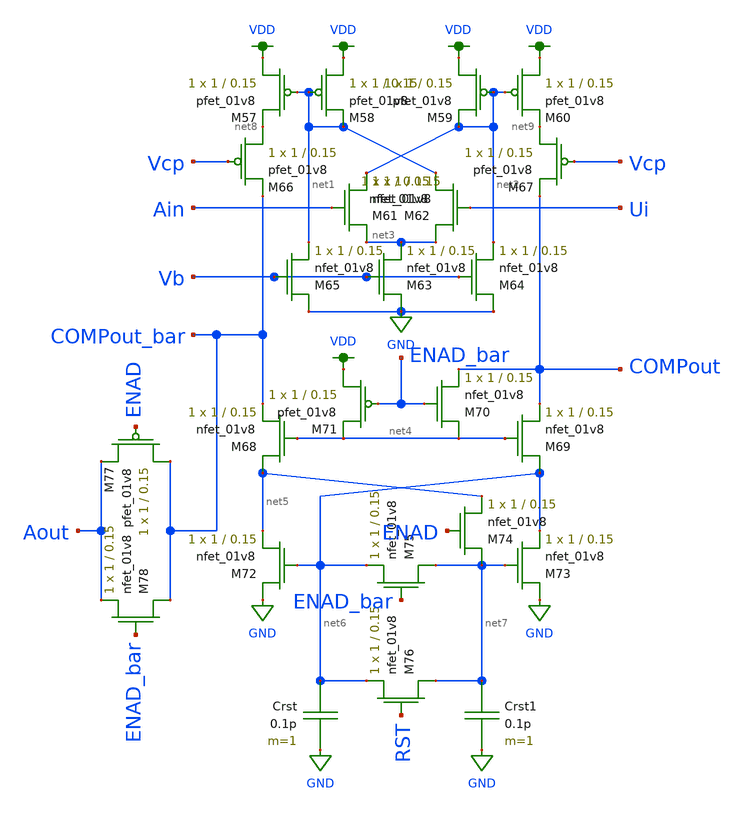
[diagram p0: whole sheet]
** sch_path: schematics/comp_report.sch
**.subckt comp_report
XM57 VDD net1 net8 VDD sky130_fd_pr__pfet_01v8 L=0.15 W=1 nf=1 ad='int((nf+1)/2) * W/nf * 0.29' as='int((nf+2)/2) * W/nf * 0.29'
+ pd='2*int((nf+1)/2) * (W/nf + 0.29)' ps='2*int((nf+2)/2) * (W/nf + 0.29)' nrd='0.29 / W' nrs='0.29 / W'
+ sa=0 sb=0 sd=0 mult=1 m=1
XM58 VDD net1 net1 VDD sky130_fd_pr__pfet_01v8 L=0.15 W=1 nf=1 ad='int((nf+1)/2) * W/nf * 0.29' as='int((nf+2)/2) * W/nf * 0.29'
+ pd='2*int((nf+1)/2) * (W/nf + 0.29)' ps='2*int((nf+2)/2) * (W/nf + 0.29)' nrd='0.29 / W' nrs='0.29 / W'
+ sa=0 sb=0 sd=0 mult=1 m=1
XM59 VDD net2 net2 VDD sky130_fd_pr__pfet_01v8 L=0.15 W=1 nf=1 ad='int((nf+1)/2) * W/nf * 0.29' as='int((nf+2)/2) * W/nf * 0.29'
+ pd='2*int((nf+1)/2) * (W/nf + 0.29)' ps='2*int((nf+2)/2) * (W/nf + 0.29)' nrd='0.29 / W' nrs='0.29 / W'
+ sa=0 sb=0 sd=0 mult=1 m=1
XM60 VDD net2 net9 VDD sky130_fd_pr__pfet_01v8 L=0.15 W=1 nf=1 ad='int((nf+1)/2) * W/nf * 0.29' as='int((nf+2)/2) * W/nf * 0.29'
+ pd='2*int((nf+1)/2) * (W/nf + 0.29)' ps='2*int((nf+2)/2) * (W/nf + 0.29)' nrd='0.29 / W' nrs='0.29 / W'
+ sa=0 sb=0 sd=0 mult=1 m=1
XM61 net3 Ain net2 GND sky130_fd_pr__nfet_01v8 L=0.15 W=1 nf=1 ad='int((nf+1)/2) * W/nf * 0.29' as='int((nf+2)/2) * W/nf * 0.29'
+ pd='2*int((nf+1)/2) * (W/nf + 0.29)' ps='2*int((nf+2)/2) * (W/nf + 0.29)' nrd='0.29 / W' nrs='0.29 / W'
+ sa=0 sb=0 sd=0 mult=1 m=1
XM62 net3 Ui net1 GND sky130_fd_pr__nfet_01v8 L=0.15 W=1 nf=1 ad='int((nf+1)/2) * W/nf * 0.29' as='int((nf+2)/2) * W/nf * 0.29'
+ pd='2*int((nf+1)/2) * (W/nf + 0.29)' ps='2*int((nf+2)/2) * (W/nf + 0.29)' nrd='0.29 / W' nrs='0.29 / W'
+ sa=0 sb=0 sd=0 mult=1 m=1
XM63 GND Vb net3 GND sky130_fd_pr__nfet_01v8 L=0.15 W=1 nf=1 ad='int((nf+1)/2) * W/nf * 0.29' as='int((nf+2)/2) * W/nf * 0.29'
+ pd='2*int((nf+1)/2) * (W/nf + 0.29)' ps='2*int((nf+2)/2) * (W/nf + 0.29)' nrd='0.29 / W' nrs='0.29 / W'
+ sa=0 sb=0 sd=0 mult=1 m=1
XM64 GND Vb net2 GND sky130_fd_pr__nfet_01v8 L=0.15 W=1 nf=1 ad='int((nf+1)/2) * W/nf * 0.29' as='int((nf+2)/2) * W/nf * 0.29'
+ pd='2*int((nf+1)/2) * (W/nf + 0.29)' ps='2*int((nf+2)/2) * (W/nf + 0.29)' nrd='0.29 / W' nrs='0.29 / W'
+ sa=0 sb=0 sd=0 mult=1 m=1
XM65 GND Vb net1 GND sky130_fd_pr__nfet_01v8 L=0.15 W=1 nf=1 ad='int((nf+1)/2) * W/nf * 0.29' as='int((nf+2)/2) * W/nf * 0.29'
+ pd='2*int((nf+1)/2) * (W/nf + 0.29)' ps='2*int((nf+2)/2) * (W/nf + 0.29)' nrd='0.29 / W' nrs='0.29 / W'
+ sa=0 sb=0 sd=0 mult=1 m=1
XM66 net8 Vcp COMPout_bar VDD sky130_fd_pr__pfet_01v8 L=0.15 W=1 nf=1 ad='int((nf+1)/2) * W/nf * 0.29'
+ as='int((nf+2)/2) * W/nf * 0.29' pd='2*int((nf+1)/2) * (W/nf + 0.29)' ps='2*int((nf+2)/2) * (W/nf + 0.29)'
+ nrd='0.29 / W' nrs='0.29 / W' sa=0 sb=0 sd=0 mult=1 m=1
XM67 net9 Vcp COMPout VDD sky130_fd_pr__pfet_01v8 L=0.15 W=1 nf=1 ad='int((nf+1)/2) * W/nf * 0.29' as='int((nf+2)/2) * W/nf * 0.29'
+ pd='2*int((nf+1)/2) * (W/nf + 0.29)' ps='2*int((nf+2)/2) * (W/nf + 0.29)' nrd='0.29 / W' nrs='0.29 / W'
+ sa=0 sb=0 sd=0 mult=1 m=1
XM68 net5 net4 COMPout_bar GND sky130_fd_pr__nfet_01v8 L=0.15 W=1 nf=1 ad='int((nf+1)/2) * W/nf * 0.29'
+ as='int((nf+2)/2) * W/nf * 0.29' pd='2*int((nf+1)/2) * (W/nf + 0.29)' ps='2*int((nf+2)/2) * (W/nf + 0.29)'
+ nrd='0.29 / W' nrs='0.29 / W' sa=0 sb=0 sd=0 mult=1 m=1
XM69 net6 net4 COMPout GND sky130_fd_pr__nfet_01v8 L=0.15 W=1 nf=1 ad='int((nf+1)/2) * W/nf * 0.29' as='int((nf+2)/2) * W/nf * 0.29'
+ pd='2*int((nf+1)/2) * (W/nf + 0.29)' ps='2*int((nf+2)/2) * (W/nf + 0.29)' nrd='0.29 / W' nrs='0.29 / W'
+ sa=0 sb=0 sd=0 mult=1 m=1
XM70 net4 ENAD_bar COMPout GND sky130_fd_pr__nfet_01v8 L=0.15 W=1 nf=1 ad='int((nf+1)/2) * W/nf * 0.29'
+ as='int((nf+2)/2) * W/nf * 0.29' pd='2*int((nf+1)/2) * (W/nf + 0.29)' ps='2*int((nf+2)/2) * (W/nf + 0.29)'
+ nrd='0.29 / W' nrs='0.29 / W' sa=0 sb=0 sd=0 mult=1 m=1
XM71 VDD ENAD_bar net4 VDD sky130_fd_pr__pfet_01v8 L=0.15 W=1 nf=1 ad='int((nf+1)/2) * W/nf * 0.29' as='int((nf+2)/2) * W/nf * 0.29'
+ pd='2*int((nf+1)/2) * (W/nf + 0.29)' ps='2*int((nf+2)/2) * (W/nf + 0.29)' nrd='0.29 / W' nrs='0.29 / W'
+ sa=0 sb=0 sd=0 mult=1 m=1
XM72 GND net6 net5 GND sky130_fd_pr__nfet_01v8 L=0.15 W=1 nf=1 ad='int((nf+1)/2) * W/nf * 0.29' as='int((nf+2)/2) * W/nf * 0.29'
+ pd='2*int((nf+1)/2) * (W/nf + 0.29)' ps='2*int((nf+2)/2) * (W/nf + 0.29)' nrd='0.29 / W' nrs='0.29 / W'
+ sa=0 sb=0 sd=0 mult=1 m=1
XM73 GND net7 net6 GND sky130_fd_pr__nfet_01v8 L=0.15 W=1 nf=1 ad='int((nf+1)/2) * W/nf * 0.29' as='int((nf+2)/2) * W/nf * 0.29'
+ pd='2*int((nf+1)/2) * (W/nf + 0.29)' ps='2*int((nf+2)/2) * (W/nf + 0.29)' nrd='0.29 / W' nrs='0.29 / W'
+ sa=0 sb=0 sd=0 mult=1 m=1
XM74 net7 ENAD net5 GND sky130_fd_pr__nfet_01v8 L=0.15 W=1 nf=1 ad='int((nf+1)/2) * W/nf * 0.29' as='int((nf+2)/2) * W/nf * 0.29'
+ pd='2*int((nf+1)/2) * (W/nf + 0.29)' ps='2*int((nf+2)/2) * (W/nf + 0.29)' nrd='0.29 / W' nrs='0.29 / W'
+ sa=0 sb=0 sd=0 mult=1 m=1
XM75 net7 ENAD_bar net6 GND sky130_fd_pr__nfet_01v8 L=0.15 W=1 nf=1 ad='int((nf+1)/2) * W/nf * 0.29'
+ as='int((nf+2)/2) * W/nf * 0.29' pd='2*int((nf+1)/2) * (W/nf + 0.29)' ps='2*int((nf+2)/2) * (W/nf + 0.29)'
+ nrd='0.29 / W' nrs='0.29 / W' sa=0 sb=0 sd=0 mult=1 m=1
Crst net6 GND 0.1p m=1
XM76 net7 RST net6 GND sky130_fd_pr__nfet_01v8 L=0.15 W=1 nf=1 ad='int((nf+1)/2) * W/nf * 0.29' as='int((nf+2)/2) * W/nf * 0.29'
+ pd='2*int((nf+1)/2) * (W/nf + 0.29)' ps='2*int((nf+2)/2) * (W/nf + 0.29)' nrd='0.29 / W' nrs='0.29 / W'
+ sa=0 sb=0 sd=0 mult=1 m=1
Crst1 net7 GND 0.1p m=1
XM77 COMPout_bar ENAD Aout VDD sky130_fd_pr__pfet_01v8 L=0.15 W=1 nf=1 ad='int((nf+1)/2) * W/nf * 0.29'
+ as='int((nf+2)/2) * W/nf * 0.29' pd='2*int((nf+1)/2) * (W/nf + 0.29)' ps='2*int((nf+2)/2) * (W/nf + 0.29)'
+ nrd='0.29 / W' nrs='0.29 / W' sa=0 sb=0 sd=0 mult=1 m=1
XM78 COMPout_bar ENAD_bar Aout GND sky130_fd_pr__nfet_01v8 L=0.15 W=1 nf=1 ad='int((nf+1)/2) * W/nf * 0.29'
+ as='int((nf+2)/2) * W/nf * 0.29' pd='2*int((nf+1)/2) * (W/nf + 0.29)' ps='2*int((nf+2)/2) * (W/nf + 0.29)'
+ nrd='0.29 / W' nrs='0.29 / W' sa=0 sb=0 sd=0 mult=1 m=1
**.ends
.GLOBAL VDD
.GLOBAL GND
.end
